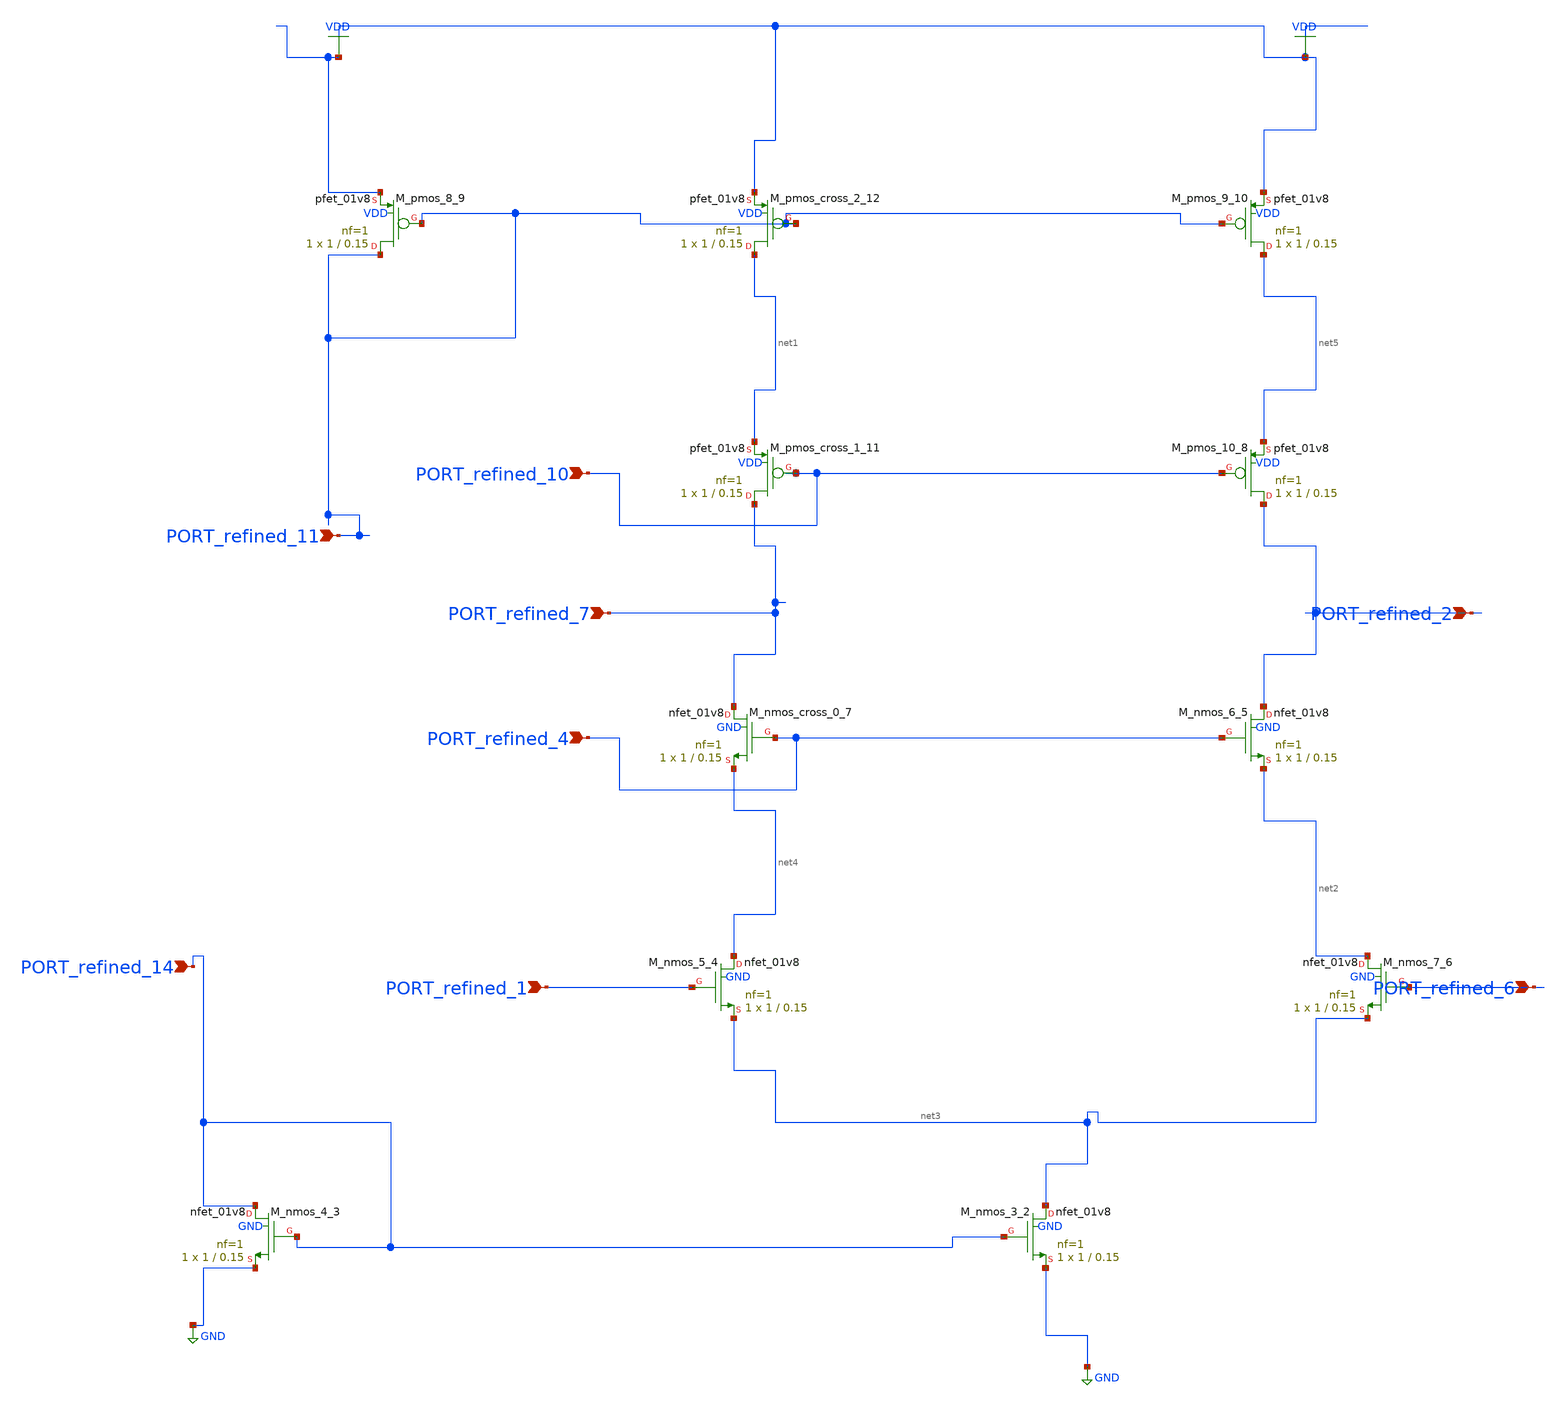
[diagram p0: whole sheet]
** sch_path: schematics/AMSNet/746.sch
**.subckt 746 PORT_refined_10 PORT_refined_2 PORT_refined_4 PORT_refined_7 PORT_refined_6
*+ PORT_refined_1 PORT_refined_14 PORT_refined_11
*.ipin PORT_refined_10
*.ipin PORT_refined_2
*.ipin PORT_refined_4
*.ipin PORT_refined_7
*.ipin PORT_refined_6
*.ipin PORT_refined_1
*.ipin PORT_refined_14
*.ipin PORT_refined_11
XM_nmos_3_2 net3 PORT_refined_14 GND GND sky130_fd_pr__nfet_01v8 L=0.15 W=1 nf=1 ad='int((1 + 1)/2) * 1 / 1 * 0.29'
+ as='int((1 + 2)/2) * 1 / 1 * 0.29' pd='2*int((1 + 1)/2) * (1 / 1 + 0.29)' ps='2*int((1 + 2)/2) * (1 / 1 + 0.29)'
+ nrd='0.29 / 1 ' nrs='0.29 / 1 ' sa=0 sb=0 sd=0 mult=1 m=1
XM_nmos_4_3 PORT_refined_14 PORT_refined_14 GND GND sky130_fd_pr__nfet_01v8 L=0.15 W=1 nf=1 ad='int((1 + 1)/2) * 1 / 1 * 0.29'
+ as='int((1 + 2)/2) * 1 / 1 * 0.29' pd='2*int((1 + 1)/2) * (1 / 1 + 0.29)' ps='2*int((1 + 2)/2) * (1 / 1 + 0.29)'
+ nrd='0.29 / 1 ' nrs='0.29 / 1 ' sa=0 sb=0 sd=0 mult=1 m=1
XM_nmos_5_4 net4 PORT_refined_1 net3 GND sky130_fd_pr__nfet_01v8 L=0.15 W=1 nf=1 ad='int((1 + 1)/2) * 1 / 1 * 0.29'
+ as='int((1 + 2)/2) * 1 / 1 * 0.29' pd='2*int((1 + 1)/2) * (1 / 1 + 0.29)' ps='2*int((1 + 2)/2) * (1 / 1 + 0.29)'
+ nrd='0.29 / 1 ' nrs='0.29 / 1 ' sa=0 sb=0 sd=0 mult=1 m=1
XM_nmos_6_5 PORT_refined_2 PORT_refined_4 net2 GND sky130_fd_pr__nfet_01v8 L=0.15 W=1 nf=1 ad='int((1 + 1)/2) * 1 / 1 * 0.29'
+ as='int((1 + 2)/2) * 1 / 1 * 0.29' pd='2*int((1 + 1)/2) * (1 / 1 + 0.29)' ps='2*int((1 + 2)/2) * (1 / 1 + 0.29)'
+ nrd='0.29 / 1 ' nrs='0.29 / 1 ' sa=0 sb=0 sd=0 mult=1 m=1
XM_nmos_7_6 net2 PORT_refined_6 net3 GND sky130_fd_pr__nfet_01v8 L=0.15 W=1 nf=1 ad='int((1 + 1)/2) * 1 / 1 * 0.29'
+ as='int((1 + 2)/2) * 1 / 1 * 0.29' pd='2*int((1 + 1)/2) * (1 / 1 + 0.29)' ps='2*int((1 + 2)/2) * (1 / 1 + 0.29)'
+ nrd='0.29 / 1 ' nrs='0.29 / 1 ' sa=0 sb=0 sd=0 mult=1 m=1
XM_nmos_cross_0_7 PORT_refined_7 PORT_refined_4 net4 GND sky130_fd_pr__nfet_01v8 L=0.15 W=1 nf=1 ad='int((1 + 1)/2) * 1 / 1 * 0.29'
+ as='int((1 + 2)/2) * 1 / 1 * 0.29' pd='2*int((1 + 1)/2) * (1 / 1 + 0.29)' ps='2*int((1 + 2)/2) * (1 / 1 + 0.29)'
+ nrd='0.29 / 1 ' nrs='0.29 / 1 ' sa=0 sb=0 sd=0 mult=1 m=1
XM_pmos_10_8 PORT_refined_2 PORT_refined_10 net5 VDD sky130_fd_pr__pfet_01v8 L=0.15 W=1 nf=1 ad='int((1 + 1)/2) * 1 / 1 * 0.29'
+ as='int((1 + 2)/2) * 1 / 1 * 0.29' pd='2*int((1 + 1)/2) * (1 / 1 + 0.29)' ps='2*int((1 + 2)/2) * (1 / 1 + 0.29)'
+ nrd='0.29 / 1 ' nrs='0.29 / 1 ' sa=0 sb=0 sd=0 mult=1 m=1
XM_pmos_8_9 PORT_refined_11 PORT_refined_11 VDD VDD sky130_fd_pr__pfet_01v8 L=0.15 W=1 nf=1 ad='int((1 + 1)/2) * 1 / 1 * 0.29'
+ as='int((1 + 2)/2) * 1 / 1 * 0.29' pd='2*int((1 + 1)/2) * (1 / 1 + 0.29)' ps='2*int((1 + 2)/2) * (1 / 1 + 0.29)'
+ nrd='0.29 / 1 ' nrs='0.29 / 1 ' sa=0 sb=0 sd=0 mult=1 m=1
XM_pmos_9_10 net5 PORT_refined_11 VDD VDD sky130_fd_pr__pfet_01v8 L=0.15 W=1 nf=1 ad='int((1 + 1)/2) * 1 / 1 * 0.29'
+ as='int((1 + 2)/2) * 1 / 1 * 0.29' pd='2*int((1 + 1)/2) * (1 / 1 + 0.29)' ps='2*int((1 + 2)/2) * (1 / 1 + 0.29)'
+ nrd='0.29 / 1 ' nrs='0.29 / 1 ' sa=0 sb=0 sd=0 mult=1 m=1
XM_pmos_cross_1_11 PORT_refined_7 PORT_refined_10 net1 VDD sky130_fd_pr__pfet_01v8 L=0.15 W=1 nf=1 ad='int((1 + 1)/2) * 1 / 1 * 0.29'
+ as='int((1 + 2)/2) * 1 / 1 * 0.29' pd='2*int((1 + 1)/2) * (1 / 1 + 0.29)' ps='2*int((1 + 2)/2) * (1 / 1 + 0.29)'
+ nrd='0.29 / 1 ' nrs='0.29 / 1 ' sa=0 sb=0 sd=0 mult=1 m=1
XM_pmos_cross_2_12 net1 PORT_refined_11 VDD VDD sky130_fd_pr__pfet_01v8 L=0.15 W=1 nf=1 ad='int((1 + 1)/2) * 1 / 1 * 0.29'
+ as='int((1 + 2)/2) * 1 / 1 * 0.29' pd='2*int((1 + 1)/2) * (1 / 1 + 0.29)' ps='2*int((1 + 2)/2) * (1 / 1 + 0.29)'
+ nrd='0.29 / 1 ' nrs='0.29 / 1 ' sa=0 sb=0 sd=0 mult=1 m=1
**.ends
.GLOBAL GND
.GLOBAL VDD
.end
